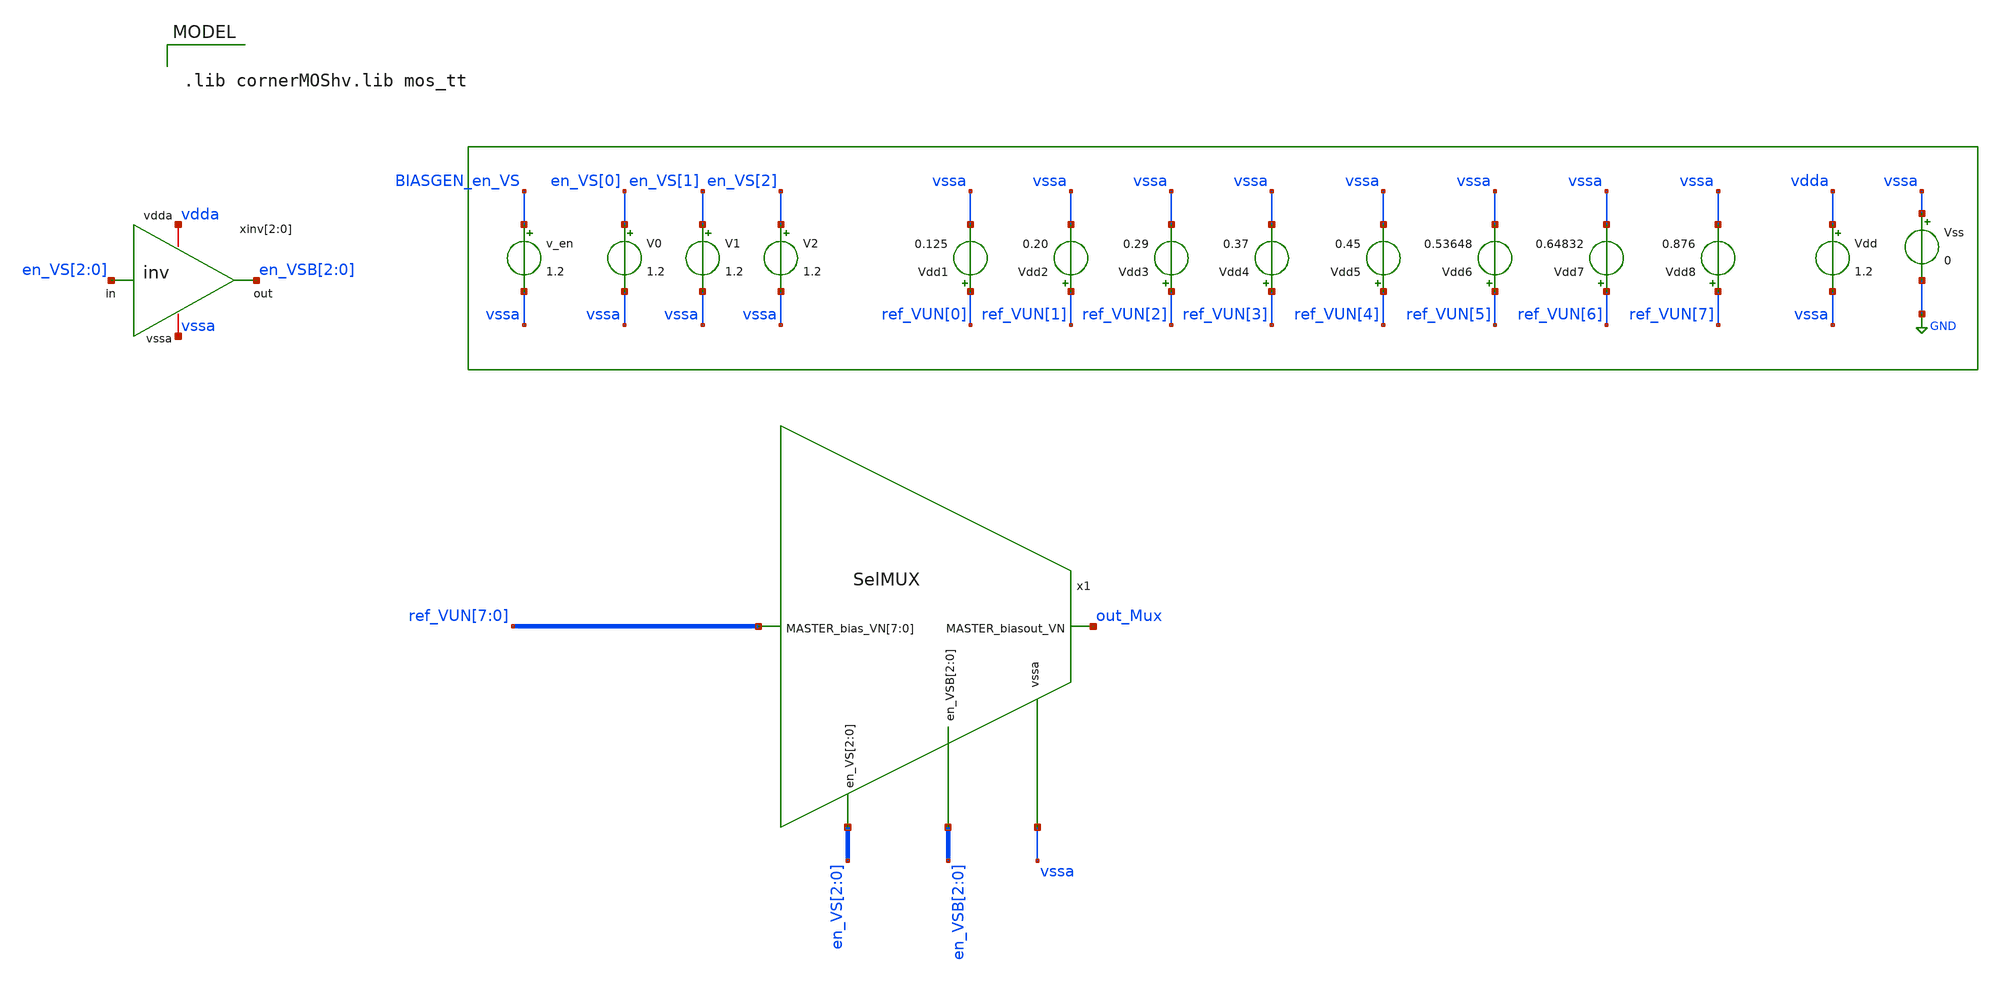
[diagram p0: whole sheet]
** sch_path: test_bench/SelMUX_alone_dc_tb.sch
**.subckt SelMUX_alone_dc_tb
v_en BIASGEN_en_VS vssa 1.2
Vdd vdda vssa 1.2
Vss vssa GND 0
xinv[2] vdda en_VSB[2] en_VS[2] vssa inv
xinv[1] vdda en_VSB[1] en_VS[1] vssa inv
xinv[0] vdda en_VSB[0] en_VS[0] vssa inv
V0 en_VS[0] vssa 1.2
V1 en_VS[1] vssa 1.2
V2 en_VS[2] vssa 1.2
x1 ref_VUN[7] ref_VUN[6] ref_VUN[5] ref_VUN[4] ref_VUN[3] ref_VUN[2] ref_VUN[1] ref_VUN[0] vssa
+ en_VS[2] en_VS[1] en_VS[0] en_VSB[2] en_VSB[1] en_VSB[0] out_Mux SelMUX
Vdd1 ref_VUN[0] vssa 0.125
Vdd2 ref_VUN[1] vssa 0.20
Vdd3 ref_VUN[2] vssa 0.29
Vdd4 ref_VUN[3] vssa 0.37
Vdd5 ref_VUN[4] vssa 0.45
Vdd6 ref_VUN[5] vssa 0.53648
Vdd7 ref_VUN[6] vssa 0.64832
Vdd8 ref_VUN[7] vssa 0.876
**** begin user architecture code

.lib cornerMOShv.lib mos_tt



.param temp=27

.options abstol=1e-13
.options gmin=1e-13
.control
save all
let digitalCommand = vector(8)
let BIAS_UN = vector(8)

let code = 0

while code < 8
    * Set the 8 bits
    alter V0 = 1.2*(code % 2)
    alter V1 = 1.2*(floor(code/2) % 2)
    alter V2 = 1.2*(floor(code/4) % 2)
    op
    let digitalCommand[code] = code
    let BIAS_UN[code]   = i(v.x1.V_ref_u_5)
    let code = code + 1
    write SelMux_alone_cases/SelMux_alone_case_{$&code}.raw
end


    setplot const
    settype current BIAS_UN
    setscale digitalCommand
    plot BIAS_UN

    write SelMUC_alone_dc_tb.raw BIAS_UN

.endc


**** end user architecture code
**.ends
.GLOBAL GND
.end
